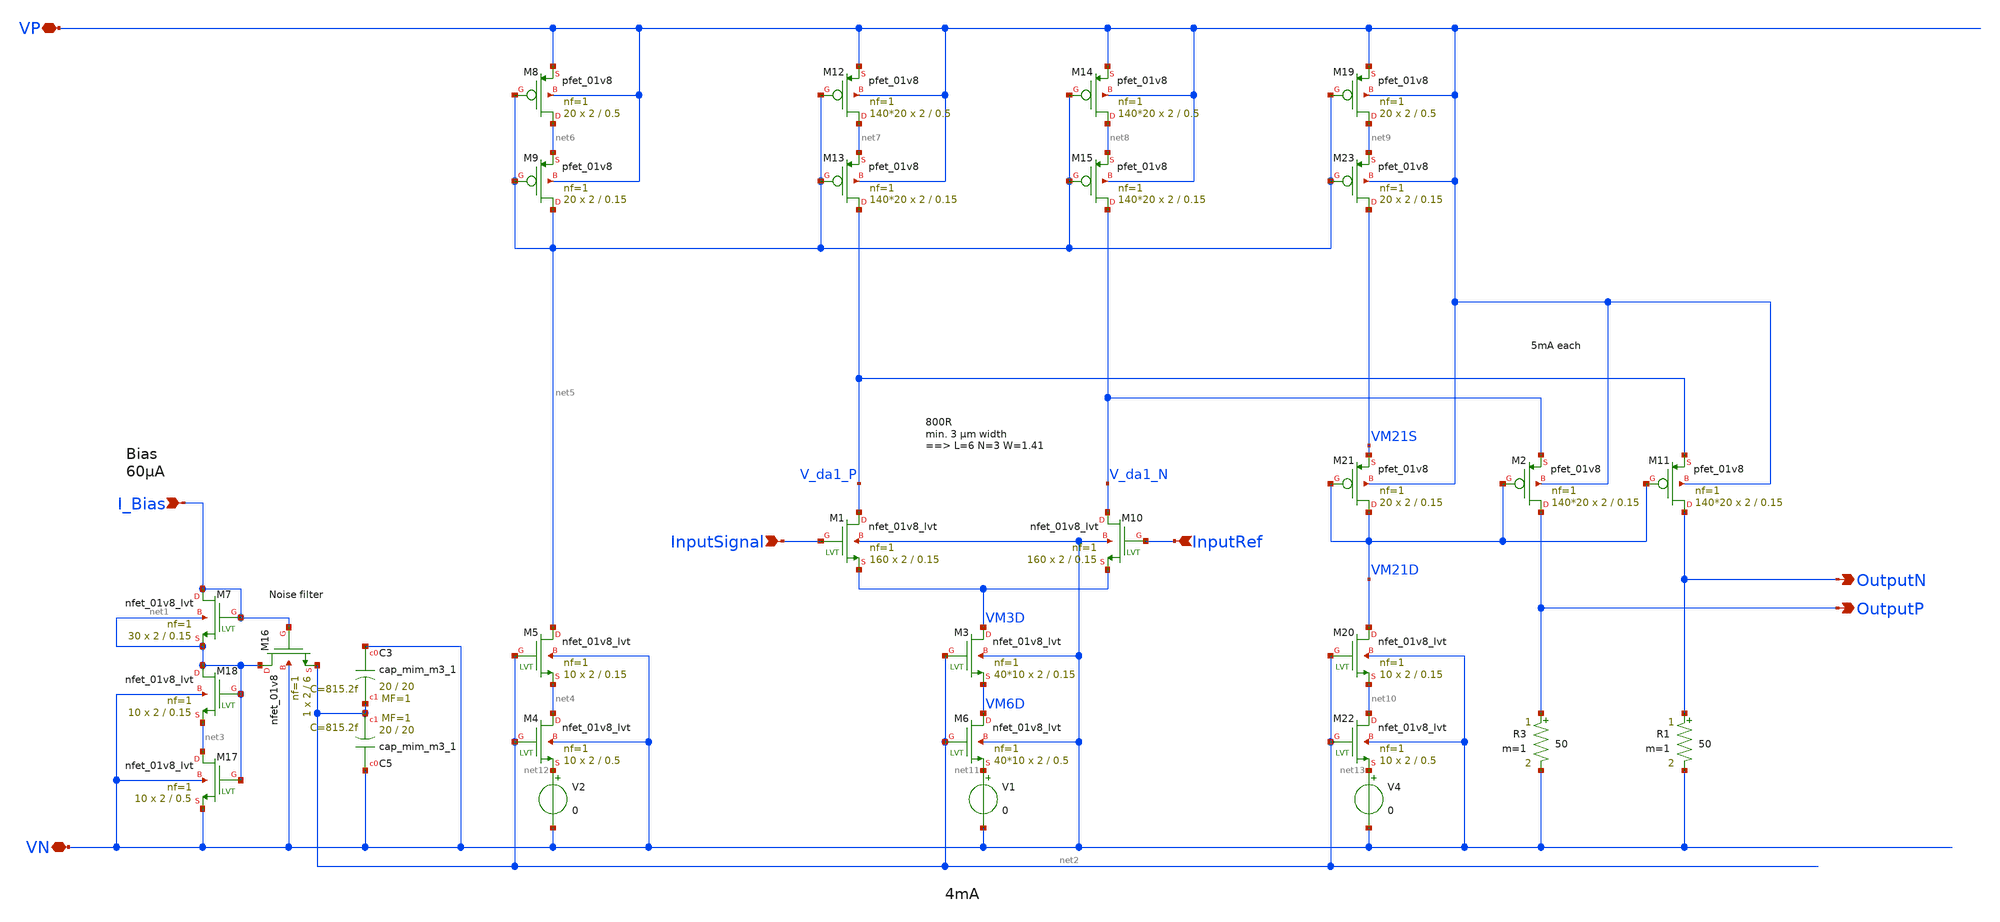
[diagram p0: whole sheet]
** sch_path: xschem/outdriver/outdriver_cascode.sch
**.subckt outdriver_cascode VN InputRef VP I_Bias InputSignal OutputN OutputP
*.iopin VN
*.ipin InputRef
*.iopin VP
*.ipin I_Bias
*.ipin InputSignal
*.opin OutputN
*.opin OutputP
XC5 VN net2 sky130_fd_pr__cap_mim_m3_1 W=20 L=20 MF=1 m=1
XC3 VN net2 sky130_fd_pr__cap_mim_m3_1 W=20 L=20 MF=1 m=1
V1 net11 VN 0
XM16 net1 I_Bias net2 VN sky130_fd_pr__nfet_01v8 L=6 W=2 nf=1 ad='int((nf+1)/2) * W/nf * 0.29' as='int((nf+2)/2) * W/nf * 0.29'
+ pd='2*int((nf+1)/2) * (W/nf + 0.29)' ps='2*int((nf+2)/2) * (W/nf + 0.29)' nrd='0.29 / W' nrs='0.29 / W'
+ sa=0 sb=0 sd=0 mult=1 m=1
XM17 net3 net1 VN VN sky130_fd_pr__nfet_01v8_lvt L=0.5 W=2 nf=1 ad='int((nf+1)/2) * W/nf * 0.29' as='int((nf+2)/2) * W/nf * 0.29'
+ pd='2*int((nf+1)/2) * (W/nf + 0.29)' ps='2*int((nf+2)/2) * (W/nf + 0.29)' nrd='0.29 / W' nrs='0.29 / W'
+ sa=0 sb=0 sd=0 mult=10 m=10
XM18 net1 net1 net3 VN sky130_fd_pr__nfet_01v8_lvt L=0.15 W=2 nf=1 ad='int((nf+1)/2) * W/nf * 0.29' as='int((nf+2)/2) * W/nf * 0.29'
+ pd='2*int((nf+1)/2) * (W/nf + 0.29)' ps='2*int((nf+2)/2) * (W/nf + 0.29)' nrd='0.29 / W' nrs='0.29 / W'
+ sa=0 sb=0 sd=0 mult=10 m=10
XM7 I_Bias I_Bias net1 net1 sky130_fd_pr__nfet_01v8_lvt L=0.15 W=2 nf=1 ad='int((nf+1)/2) * W/nf * 0.29'
+ as='int((nf+2)/2) * W/nf * 0.29' pd='2*int((nf+1)/2) * (W/nf + 0.29)' ps='2*int((nf+2)/2) * (W/nf + 0.29)'
+ nrd='0.29 / W' nrs='0.29 / W' sa=0 sb=0 sd=0 mult=30 m=30
XM1 V_da1_P InputSignal VM3D VN sky130_fd_pr__nfet_01v8_lvt L=0.15 W=2 nf=1 ad='int((nf+1)/2) * W/nf * 0.29'
+ as='int((nf+2)/2) * W/nf * 0.29' pd='2*int((nf+1)/2) * (W/nf + 0.29)' ps='2*int((nf+2)/2) * (W/nf + 0.29)'
+ nrd='0.29 / W' nrs='0.29 / W' sa=0 sb=0 sd=0 mult=160 m=160
XM3 VM3D net2 VM6D VN sky130_fd_pr__nfet_01v8_lvt L=0.15 W=2 nf=1 ad='int((nf+1)/2) * W/nf * 0.29' as='int((nf+2)/2) * W/nf * 0.29'
+ pd='2*int((nf+1)/2) * (W/nf + 0.29)' ps='2*int((nf+2)/2) * (W/nf + 0.29)' nrd='0.29 / W' nrs='0.29 / W'
+ sa=0 sb=0 sd=0 mult=40*10 m=40*10
R3 OutputP VN 50 m=1
XM2 OutputP VM21D V_da1_N VP sky130_fd_pr__pfet_01v8 L=0.15 W=2 nf=1 ad='int((nf+1)/2) * W/nf * 0.29'
+ as='int((nf+2)/2) * W/nf * 0.29' pd='2*int((nf+1)/2) * (W/nf + 0.29)' ps='2*int((nf+2)/2) * (W/nf + 0.29)'
+ nrd='0.29 / W' nrs='0.29 / W' sa=0 sb=0 sd=0 mult=140*20 m=140*20
V2 net12 VN 0
XM8 net6 net5 VP VP sky130_fd_pr__pfet_01v8 L=0.5 W=2 nf=1 ad='int((nf+1)/2) * W/nf * 0.29' as='int((nf+2)/2) * W/nf * 0.29'
+ pd='2*int((nf+1)/2) * (W/nf + 0.29)' ps='2*int((nf+2)/2) * (W/nf + 0.29)' nrd='0.29 / W' nrs='0.29 / W'
+ sa=0 sb=0 sd=0 mult=20 m=20
XM9 net5 net5 net6 VP sky130_fd_pr__pfet_01v8 L=0.15 W=2 nf=1 ad='int((nf+1)/2) * W/nf * 0.29' as='int((nf+2)/2) * W/nf * 0.29'
+ pd='2*int((nf+1)/2) * (W/nf + 0.29)' ps='2*int((nf+2)/2) * (W/nf + 0.29)' nrd='0.29 / W' nrs='0.29 / W'
+ sa=0 sb=0 sd=0 mult=20 m=20
XM11 OutputN VM21D V_da1_P VP sky130_fd_pr__pfet_01v8 L=0.15 W=2 nf=1 ad='int((nf+1)/2) * W/nf * 0.29'
+ as='int((nf+2)/2) * W/nf * 0.29' pd='2*int((nf+1)/2) * (W/nf + 0.29)' ps='2*int((nf+2)/2) * (W/nf + 0.29)'
+ nrd='0.29 / W' nrs='0.29 / W' sa=0 sb=0 sd=0 mult=140*20 m=140*20
XM21 VM21D VM21D VM21S VP sky130_fd_pr__pfet_01v8 L=0.15 W=2 nf=1 ad='int((nf+1)/2) * W/nf * 0.29' as='int((nf+2)/2) * W/nf * 0.29'
+ pd='2*int((nf+1)/2) * (W/nf + 0.29)' ps='2*int((nf+2)/2) * (W/nf + 0.29)' nrd='0.29 / W' nrs='0.29 / W'
+ sa=0 sb=0 sd=0 mult=20 m=20
R1 OutputN VN 50 m=1
V4 net13 VN 0
XM10 V_da1_N InputRef VM3D VN sky130_fd_pr__nfet_01v8_lvt L=0.15 W=2 nf=1 ad='int((nf+1)/2) * W/nf * 0.29'
+ as='int((nf+2)/2) * W/nf * 0.29' pd='2*int((nf+1)/2) * (W/nf + 0.29)' ps='2*int((nf+2)/2) * (W/nf + 0.29)'
+ nrd='0.29 / W' nrs='0.29 / W' sa=0 sb=0 sd=0 mult=160 m=160
XM4 net4 net2 net12 VN sky130_fd_pr__nfet_01v8_lvt L=0.5 W=2 nf=1 ad='int((nf+1)/2) * W/nf * 0.29' as='int((nf+2)/2) * W/nf * 0.29'
+ pd='2*int((nf+1)/2) * (W/nf + 0.29)' ps='2*int((nf+2)/2) * (W/nf + 0.29)' nrd='0.29 / W' nrs='0.29 / W'
+ sa=0 sb=0 sd=0 mult=10 m=10
XM5 net5 net2 net4 VN sky130_fd_pr__nfet_01v8_lvt L=0.15 W=2 nf=1 ad='int((nf+1)/2) * W/nf * 0.29' as='int((nf+2)/2) * W/nf * 0.29'
+ pd='2*int((nf+1)/2) * (W/nf + 0.29)' ps='2*int((nf+2)/2) * (W/nf + 0.29)' nrd='0.29 / W' nrs='0.29 / W'
+ sa=0 sb=0 sd=0 mult=10 m=10
XM6 VM6D net2 net11 VN sky130_fd_pr__nfet_01v8_lvt L=0.5 W=2 nf=1 ad='int((nf+1)/2) * W/nf * 0.29' as='int((nf+2)/2) * W/nf * 0.29'
+ pd='2*int((nf+1)/2) * (W/nf + 0.29)' ps='2*int((nf+2)/2) * (W/nf + 0.29)' nrd='0.29 / W' nrs='0.29 / W'
+ sa=0 sb=0 sd=0 mult=40*10 m=40*10
XM20 VM21D net2 net10 VN sky130_fd_pr__nfet_01v8_lvt L=0.15 W=2 nf=1 ad='int((nf+1)/2) * W/nf * 0.29'
+ as='int((nf+2)/2) * W/nf * 0.29' pd='2*int((nf+1)/2) * (W/nf + 0.29)' ps='2*int((nf+2)/2) * (W/nf + 0.29)'
+ nrd='0.29 / W' nrs='0.29 / W' sa=0 sb=0 sd=0 mult=10 m=10
XM22 net10 net2 net13 VN sky130_fd_pr__nfet_01v8_lvt L=0.5 W=2 nf=1 ad='int((nf+1)/2) * W/nf * 0.29'
+ as='int((nf+2)/2) * W/nf * 0.29' pd='2*int((nf+1)/2) * (W/nf + 0.29)' ps='2*int((nf+2)/2) * (W/nf + 0.29)'
+ nrd='0.29 / W' nrs='0.29 / W' sa=0 sb=0 sd=0 mult=10 m=10
XM13 V_da1_P net5 net7 VP sky130_fd_pr__pfet_01v8 L=0.15 W=2 nf=1 ad='int((nf+1)/2) * W/nf * 0.29' as='int((nf+2)/2) * W/nf * 0.29'
+ pd='2*int((nf+1)/2) * (W/nf + 0.29)' ps='2*int((nf+2)/2) * (W/nf + 0.29)' nrd='0.29 / W' nrs='0.29 / W'
+ sa=0 sb=0 sd=0 mult=140*20 m=140*20
XM15 V_da1_N net5 net8 VP sky130_fd_pr__pfet_01v8 L=0.15 W=2 nf=1 ad='int((nf+1)/2) * W/nf * 0.29' as='int((nf+2)/2) * W/nf * 0.29'
+ pd='2*int((nf+1)/2) * (W/nf + 0.29)' ps='2*int((nf+2)/2) * (W/nf + 0.29)' nrd='0.29 / W' nrs='0.29 / W'
+ sa=0 sb=0 sd=0 mult=140*20 m=140*20
XM12 net7 net5 VP VP sky130_fd_pr__pfet_01v8 L=0.5 W=2 nf=1 ad='int((nf+1)/2) * W/nf * 0.29' as='int((nf+2)/2) * W/nf * 0.29'
+ pd='2*int((nf+1)/2) * (W/nf + 0.29)' ps='2*int((nf+2)/2) * (W/nf + 0.29)' nrd='0.29 / W' nrs='0.29 / W'
+ sa=0 sb=0 sd=0 mult=140*20 m=140*20
XM19 net9 net5 VP VP sky130_fd_pr__pfet_01v8 L=0.5 W=2 nf=1 ad='int((nf+1)/2) * W/nf * 0.29' as='int((nf+2)/2) * W/nf * 0.29'
+ pd='2*int((nf+1)/2) * (W/nf + 0.29)' ps='2*int((nf+2)/2) * (W/nf + 0.29)' nrd='0.29 / W' nrs='0.29 / W'
+ sa=0 sb=0 sd=0 mult=20 m=20
XM23 VM21S net5 net9 VP sky130_fd_pr__pfet_01v8 L=0.15 W=2 nf=1 ad='int((nf+1)/2) * W/nf * 0.29' as='int((nf+2)/2) * W/nf * 0.29'
+ pd='2*int((nf+1)/2) * (W/nf + 0.29)' ps='2*int((nf+2)/2) * (W/nf + 0.29)' nrd='0.29 / W' nrs='0.29 / W'
+ sa=0 sb=0 sd=0 mult=20 m=20
XM14 net8 net5 VP VP sky130_fd_pr__pfet_01v8 L=0.5 W=2 nf=1 ad='int((nf+1)/2) * W/nf * 0.29' as='int((nf+2)/2) * W/nf * 0.29'
+ pd='2*int((nf+1)/2) * (W/nf + 0.29)' ps='2*int((nf+2)/2) * (W/nf + 0.29)' nrd='0.29 / W' nrs='0.29 / W'
+ sa=0 sb=0 sd=0 mult=140*20 m=140*20
**.ends
.end
